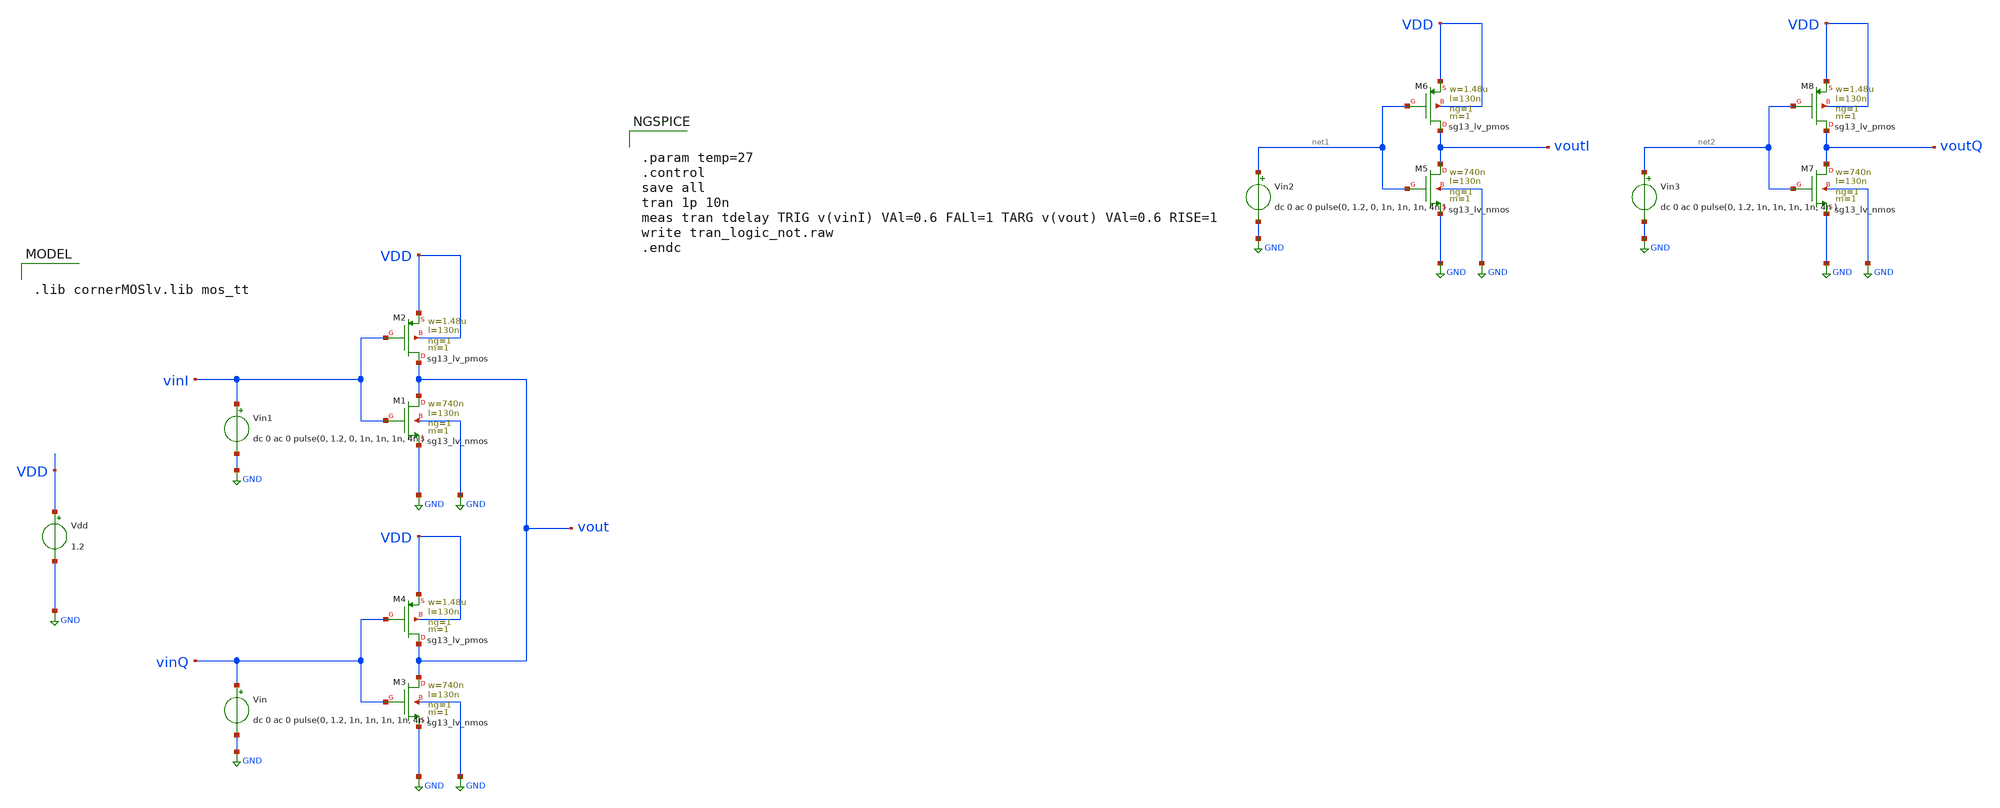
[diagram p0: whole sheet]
** sch_path: PhaseInterpolator/tb_2x_PI.sch
**.subckt tb_2x_PI
Vin vinQ GND dc 0 ac 0 pulse(0, 1.2, 1n, 1n, 1n, 1n, 4n )
Vin1 vinI GND dc 0 ac 0 pulse(0, 1.2, 0, 1n, 1n, 1n, 4n )
Vdd VDD GND 1.2
XM1 vout vinI GND GND sg13_lv_nmos w=740n l=130n ng=1 m=1 mm_ok=1
XM2 vout vinI VDD VDD sg13_lv_pmos w=1.48u l=130n ng=1 m=1 mm_ok=1
XM3 vout vinQ GND GND sg13_lv_nmos w=740n l=130n ng=1 m=1 mm_ok=1
XM4 vout vinQ VDD VDD sg13_lv_pmos w=1.48u l=130n ng=1 m=1 mm_ok=1
Vin2 net1 GND dc 0 ac 0 pulse(0, 1.2, 0, 1n, 1n, 1n, 4n )
XM5 voutI net1 GND GND sg13_lv_nmos w=740n l=130n ng=1 m=1 mm_ok=1
XM6 voutI net1 VDD VDD sg13_lv_pmos w=1.48u l=130n ng=1 m=1 mm_ok=1
Vin3 net2 GND dc 0 ac 0 pulse(0, 1.2, 1n, 1n, 1n, 1n, 4n )
XM7 voutQ net2 GND GND sg13_lv_nmos w=740n l=130n ng=1 m=1 mm_ok=1
XM8 voutQ net2 VDD VDD sg13_lv_pmos w=1.48u l=130n ng=1 m=1 mm_ok=1
**** begin user architecture code


.param temp=27
.control
save all
tran 1p 10n
meas tran tdelay TRIG v(vinI) VAl=0.6 FALl=1 TARG v(vout) VAl=0.6 RISE=1
write tran_logic_not.raw
.endc



.lib cornerMOSlv.lib mos_tt

**** end user architecture code
**.ends
.GLOBAL GND
.end
